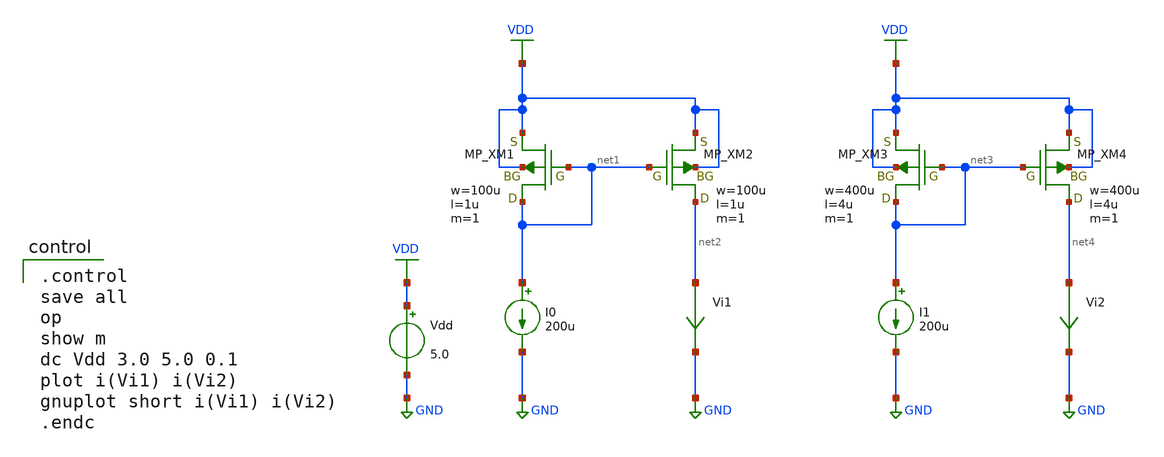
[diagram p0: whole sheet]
** sch_path: Vol.2/files/02/xschem/short_channel.sch
**.subckt short_channel
I0 net1 GND 200u
Vi1 net2 GND 0
.save i(vi1)
Vdd VDD GND 5.0
I1 net3 GND 200u
Vi2 net4 GND 0
.save i(vi2)
XM1 net1 net1 VDD VDD PMOS w=100u l=1u as=0 ad=0 ps=0 pd=0 nrd=0 nrs=0 m=1
XM2 net2 net1 VDD VDD PMOS w=100u l=1u as=0 ad=0 ps=0 pd=0 nrd=0 nrs=0 m=1
XM3 net3 net3 VDD VDD PMOS w=400u l=4u as=0 ad=0 ps=0 pd=0 nrd=0 nrs=0 m=1
XM4 net4 net3 VDD VDD PMOS w=400u l=4u as=0 ad=0 ps=0 pd=0 nrd=0 nrs=0 m=1
**** begin user architecture code

.control
save all
op
show m
dc Vdd 3.0 5.0 0.1
plot i(Vi1) i(Vi2)
gnuplot short i(Vi1) i(Vi2)
.endc

 .include $::LIB/../ip62_models
**** end user architecture code
**.ends
.GLOBAL GND
.GLOBAL VDD
.end
